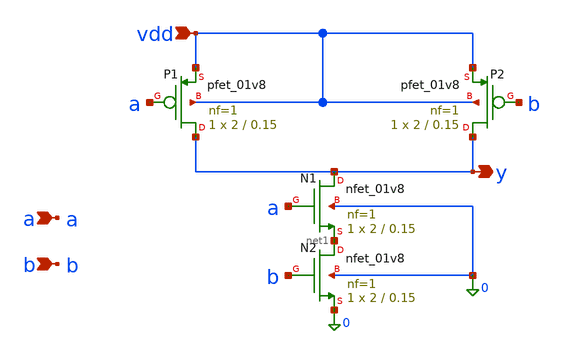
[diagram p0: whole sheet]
** sch_path: sch/nand2.sch
**.subckt nand2 a vdd y b
*.ipin a
*.ipin vdd
*.opin y
*.ipin b
XP1 y a vdd vdd sky130_fd_pr__pfet_01v8 L=0.15 W=2 nf=1 ad='int((1 + 1)/2) * 2 / 1 * 0.29' as='int((1 + 2)/2) * 2 / 1 * 0.29'
+ pd='2*int((1 + 1)/2) * (2 / 1 + 0.29)' ps='2*int((1 + 2)/2) * (2 / 1 + 0.29)' nrd='0.29 / 2 ' nrs='0.29 / 2 '
+ sa=0 sb=0 sd=0 mult=1 m=1
XP2 y b vdd vdd sky130_fd_pr__pfet_01v8 L=0.15 W=2 nf=1 ad='int((1 + 1)/2) * 2 / 1 * 0.29' as='int((1 + 2)/2) * 2 / 1 * 0.29'
+ pd='2*int((1 + 1)/2) * (2 / 1 + 0.29)' ps='2*int((1 + 2)/2) * (2 / 1 + 0.29)' nrd='0.29 / 2 ' nrs='0.29 / 2 '
+ sa=0 sb=0 sd=0 mult=1 m=1
XN1 y a net1 0 sky130_fd_pr__nfet_01v8 L=0.15 W=2 nf=1 ad='int((1 + 1)/2) * 2 / 1 * 0.29' as='int((1 + 2)/2) * 2 / 1 * 0.29'
+ pd='2*int((1 + 1)/2) * (2 / 1 + 0.29)' ps='2*int((1 + 2)/2) * (2 / 1 + 0.29)' nrd='0.29 / 2 ' nrs='0.29 / 2 '
+ sa=0 sb=0 sd=0 mult=1 m=1
XN2 net1 b 0 0 sky130_fd_pr__nfet_01v8 L=0.15 W=2 nf=1 ad='int((1 + 1)/2) * 2 / 1 * 0.29' as='int((1 + 2)/2) * 2 / 1 * 0.29'
+ pd='2*int((1 + 1)/2) * (2 / 1 + 0.29)' ps='2*int((1 + 2)/2) * (2 / 1 + 0.29)' nrd='0.29 / 2 ' nrs='0.29 / 2 '
+ sa=0 sb=0 sd=0 mult=1 m=1
**.ends
.end
